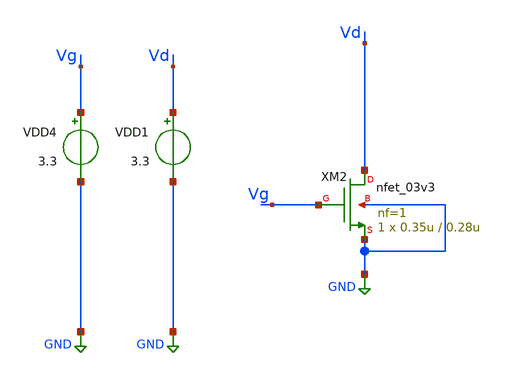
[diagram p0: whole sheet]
** sch_path: SAR_ADC/tracking_switches/xschem/on_resistance.sch
**.subckt on_resistance
XM2 Vd Vg GND GND nfet_03v3 L=0.28u W=0.35u nf=1 ad='int((nf+1)/2) * W/nf * 0.18u' as='int((nf+2)/2) * W/nf * 0.18u'
+ pd='2*int((nf+1)/2) * (W/nf + 0.18u)' ps='2*int((nf+2)/2) * (W/nf + 0.18u)' nrd='0.18u / W' nrs='0.18u / W'
+ sa=0 sb=0 sd=0 m=1
VDD4 Vg GND 3.3
VDD1 Vd GND 3.3
**** begin user architecture code



*Parameters

.options TEMP = 50.0
.lib /home/gf180/Documents/gf180/pdk/gf180mcuD/libs.tech/ngspice/sm141064.ngspice typical
.include /home/gf180/Documents/gf180/pdk/gf180mcuD/libs.tech/ngspice/design.ngspice
.lib /home/gf180/Documents/gf180/pdk/gf180mcuD/libs.tech/ngspice/sm141064.ngspice cap_mim
.lib /home/gf180/Documents/gf180/pdk/gf180mcuD/libs.tech/ngspice/sm141064.ngspice mimcap_statistical

*Data to save
.save all


* Simulation
.control

dc VDD4 0 3.3 0.01
plot -i(VDD1)

reset
unset filetype
op
save all
write on_resistance_tb.raw


.endc
.end


**** end user architecture code
**.ends
.GLOBAL GND
.end
